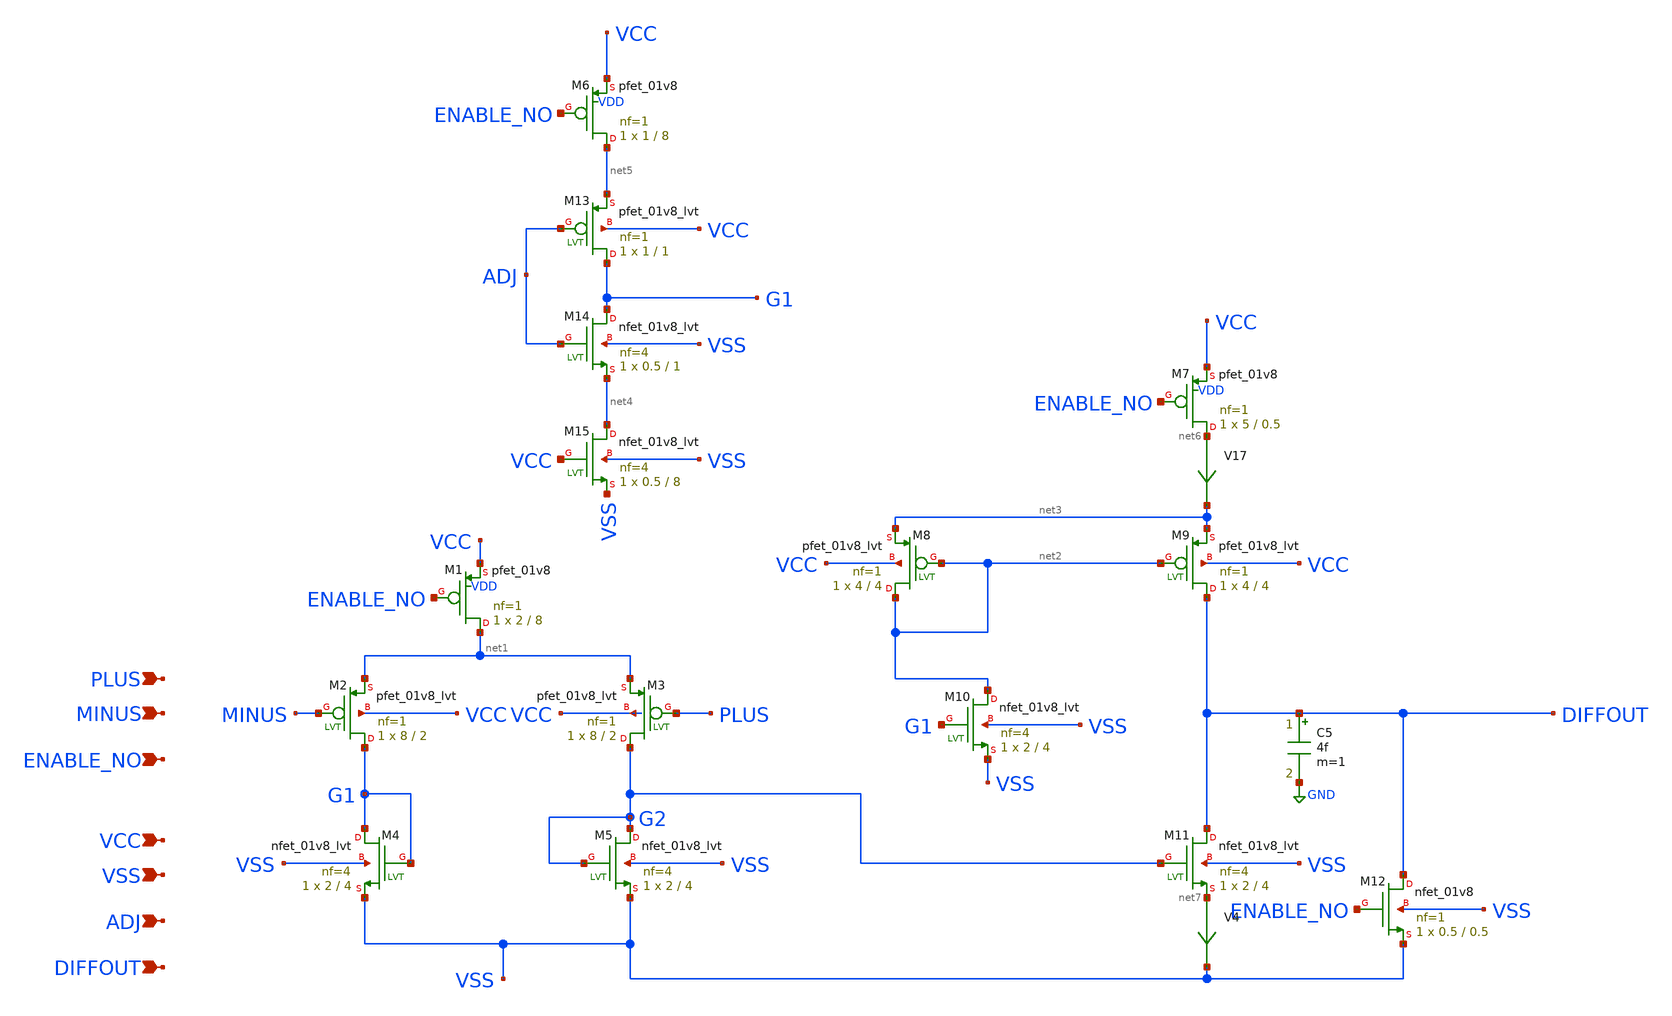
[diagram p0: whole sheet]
** sch_path: Comparador-analogico/Comparer.sch
**.subckt Comparer PLUS MINUS VCC VSS ENABLE_NO ADJ DIFFOUT
*.ipin PLUS
*.ipin MINUS
*.ipin VCC
*.ipin VSS
*.ipin ENABLE_NO
*.ipin ADJ
*.ipin DIFFOUT
XM1 net1 ENABLE_NO VCC VDD sky130_fd_pr__pfet_01v8 L=8 W=2 nf=1 ad='int((nf+1)/2) * W/nf * 0.29' as='int((nf+2)/2) * W/nf * 0.29'
+ pd='2*int((nf+1)/2) * (W/nf + 0.29)' ps='2*int((nf+2)/2) * (W/nf + 0.29)' nrd='0.29 / W' nrs='0.29 / W'
+ sa=0 sb=0 sd=0 mult=1 m=1
XM2 G1 MINUS net1 VCC sky130_fd_pr__pfet_01v8_lvt L=2 W=8 nf=1 ad='int((nf+1)/2) * W/nf * 0.29' as='int((nf+2)/2) * W/nf * 0.29'
+ pd='2*int((nf+1)/2) * (W/nf + 0.29)' ps='2*int((nf+2)/2) * (W/nf + 0.29)' nrd='0.29 / W' nrs='0.29 / W'
+ sa=0 sb=0 sd=0 mult=1 m=1
XM3 G2 PLUS net1 VCC sky130_fd_pr__pfet_01v8_lvt L=2 W=8 nf=1 ad='int((nf+1)/2) * W/nf * 0.29' as='int((nf+2)/2) * W/nf * 0.29'
+ pd='2*int((nf+1)/2) * (W/nf + 0.29)' ps='2*int((nf+2)/2) * (W/nf + 0.29)' nrd='0.29 / W' nrs='0.29 / W'
+ sa=0 sb=0 sd=0 mult=1 m=1
XM4 G1 G1 VSS VSS sky130_fd_pr__nfet_01v8_lvt L=4 W=2 nf=4 ad='int((nf+1)/2) * W/nf * 0.29' as='int((nf+2)/2) * W/nf * 0.29'
+ pd='2*int((nf+1)/2) * (W/nf + 0.29)' ps='2*int((nf+2)/2) * (W/nf + 0.29)' nrd='0.29 / W' nrs='0.29 / W'
+ sa=0 sb=0 sd=0 mult=1 m=1
XM5 G2 G2 VSS VSS sky130_fd_pr__nfet_01v8_lvt L=4 W=2 nf=4 ad='int((nf+1)/2) * W/nf * 0.29' as='int((nf+2)/2) * W/nf * 0.29'
+ pd='2*int((nf+1)/2) * (W/nf + 0.29)' ps='2*int((nf+2)/2) * (W/nf + 0.29)' nrd='0.29 / W' nrs='0.29 / W'
+ sa=0 sb=0 sd=0 mult=1 m=1
XM7 net6 ENABLE_NO VCC VDD sky130_fd_pr__pfet_01v8 L=0.5 W=5 nf=1 ad='int((nf+1)/2) * W/nf * 0.29' as='int((nf+2)/2) * W/nf * 0.29'
+ pd='2*int((nf+1)/2) * (W/nf + 0.29)' ps='2*int((nf+2)/2) * (W/nf + 0.29)' nrd='0.29 / W' nrs='0.29 / W'
+ sa=0 sb=0 sd=0 mult=1 m=1
XM8 net2 net2 net3 VCC sky130_fd_pr__pfet_01v8_lvt L=4 W=4 nf=1 ad='int((nf+1)/2) * W/nf * 0.29' as='int((nf+2)/2) * W/nf * 0.29'
+ pd='2*int((nf+1)/2) * (W/nf + 0.29)' ps='2*int((nf+2)/2) * (W/nf + 0.29)' nrd='0.29 / W' nrs='0.29 / W'
+ sa=0 sb=0 sd=0 mult=1 m=1
XM9 DIFFOUT net2 net3 VCC sky130_fd_pr__pfet_01v8_lvt L=4 W=4 nf=1 ad='int((nf+1)/2) * W/nf * 0.29' as='int((nf+2)/2) * W/nf * 0.29'
+ pd='2*int((nf+1)/2) * (W/nf + 0.29)' ps='2*int((nf+2)/2) * (W/nf + 0.29)' nrd='0.29 / W' nrs='0.29 / W'
+ sa=0 sb=0 sd=0 mult=1 m=1
XM10 net2 G1 VSS VSS sky130_fd_pr__nfet_01v8_lvt L=4 W=2 nf=4 ad='int((nf+1)/2) * W/nf * 0.29' as='int((nf+2)/2) * W/nf * 0.29'
+ pd='2*int((nf+1)/2) * (W/nf + 0.29)' ps='2*int((nf+2)/2) * (W/nf + 0.29)' nrd='0.29 / W' nrs='0.29 / W'
+ sa=0 sb=0 sd=0 mult=1 m=1
V17 net6 net3 0
.save i(v17)
XM11 DIFFOUT G2 net7 VSS sky130_fd_pr__nfet_01v8_lvt L=4 W=2 nf=4 ad='int((nf+1)/2) * W/nf * 0.29' as='int((nf+2)/2) * W/nf * 0.29'
+ pd='2*int((nf+1)/2) * (W/nf + 0.29)' ps='2*int((nf+2)/2) * (W/nf + 0.29)' nrd='0.29 / W' nrs='0.29 / W'
+ sa=0 sb=0 sd=0 mult=1 m=1
XM12 DIFFOUT ENABLE_NO VSS VSS sky130_fd_pr__nfet_01v8 L=0.5 W=0.5 nf=1 ad='int((nf+1)/2) * W/nf * 0.29'
+ as='int((nf+2)/2) * W/nf * 0.29' pd='2*int((nf+1)/2) * (W/nf + 0.29)' ps='2*int((nf+2)/2) * (W/nf + 0.29)'
+ nrd='0.29 / W' nrs='0.29 / W' sa=0 sb=0 sd=0 mult=1 m=1
V4 net7 VSS 0
.save i(v4)
C5 DIFFOUT GND 4f m=1
XM6 net5 ENABLE_NO VCC VDD sky130_fd_pr__pfet_01v8 L=8 W=1 nf=1 ad='int((nf+1)/2) * W/nf * 0.29' as='int((nf+2)/2) * W/nf * 0.29'
+ pd='2*int((nf+1)/2) * (W/nf + 0.29)' ps='2*int((nf+2)/2) * (W/nf + 0.29)' nrd='0.29 / W' nrs='0.29 / W'
+ sa=0 sb=0 sd=0 mult=1 m=1
XM13 G1 ADJ net5 VCC sky130_fd_pr__pfet_01v8_lvt L=1 W=1 nf=1 ad='int((nf+1)/2) * W/nf * 0.29' as='int((nf+2)/2) * W/nf * 0.29'
+ pd='2*int((nf+1)/2) * (W/nf + 0.29)' ps='2*int((nf+2)/2) * (W/nf + 0.29)' nrd='0.29 / W' nrs='0.29 / W'
+ sa=0 sb=0 sd=0 mult=1 m=1
XM14 G1 ADJ net4 VSS sky130_fd_pr__nfet_01v8_lvt L=1 W=0.5 nf=4 ad='int((nf+1)/2) * W/nf * 0.29' as='int((nf+2)/2) * W/nf * 0.29'
+ pd='2*int((nf+1)/2) * (W/nf + 0.29)' ps='2*int((nf+2)/2) * (W/nf + 0.29)' nrd='0.29 / W' nrs='0.29 / W'
+ sa=0 sb=0 sd=0 mult=1 m=1
XM15 net4 VCC VSS VSS sky130_fd_pr__nfet_01v8_lvt L=8 W=0.5 nf=4 ad='int((nf+1)/2) * W/nf * 0.29' as='int((nf+2)/2) * W/nf * 0.29'
+ pd='2*int((nf+1)/2) * (W/nf + 0.29)' ps='2*int((nf+2)/2) * (W/nf + 0.29)' nrd='0.29 / W' nrs='0.29 / W'
+ sa=0 sb=0 sd=0 mult=1 m=1
**.ends
.GLOBAL GND
.end
